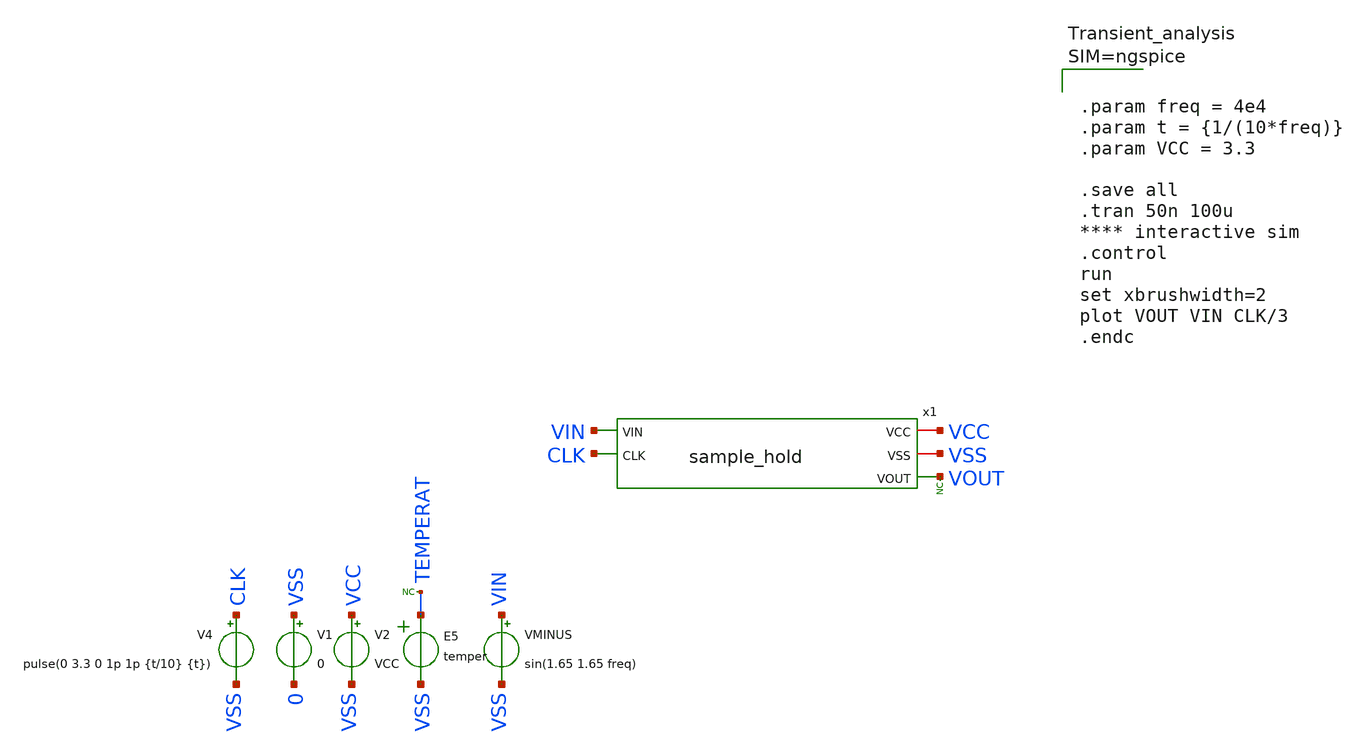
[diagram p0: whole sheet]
** sch_path: sample_hold/schematic/sample_hold_tb.sch
.lib $::SKYWATER_MODELS/sky130.lib.spice.tt.red tt
.include $::SKYWATER_STDCELLS/sky130_fd_sc_hd.spice

**.subckt sample_hold_tb
x1 VCC VSS VOUT VIN CLK sample_hold
V1 VSS 0 0
V2 VCC VSS VCC
VMINUS VIN VSS sin(1.65 1.65 freq)
E5 TEMPERAT VSS VOL=' temper '
* noconn TEMPERAT
V4 CLK VSS pulse(0 3.3 0 1p 1p {t/10} {t})
* noconn VOUT
**** begin user architecture code



.param freq = 4e4
.param t = {1/(10*freq)}
.param VCC = 3.3

.save all
.tran 50n 100u
**** interactive sim
.control
run
set xbrushwidth=2
plot VOUT VIN CLK/3
.endc



**** end user architecture code
**.ends

* expanding   symbol:  sample_hold.sym # of pins=5
** sym_path: sample_hold/schematic/sample_hold.sym
** sch_path: sample_hold/schematic/sample_hold.sch
.subckt sample_hold VCC VSS VOUT VIN CLK
*.iopin VCC
*.ipin VIN
*.opin VOUT
*.ipin CLK
*.iopin VSS
XM5 net1 net4 VCC VCC sky130_fd_pr__pfet_g5v0d10v5 L=0.5 W=1 nf=1 ad='int((nf+1)/2) * W/nf * 0.29' as='int((nf+2)/2) * W/nf * 0.29'
+ pd='2*int((nf+1)/2) * (W/nf + 0.29)' ps='2*int((nf+2)/2) * (W/nf + 0.29)' nrd='0.29 / W' nrs='0.29 / W'
+ sa=0 sb=0 sd=0 mult=1 m=1
XM6 net3 CLKN VSS VSS sky130_fd_pr__nfet_g5v0d10v5 L=0.5 W=1 nf=1 ad='int((nf+1)/2) * W/nf * 0.29' as='int((nf+2)/2) * W/nf * 0.29'
+ pd='2*int((nf+1)/2) * (W/nf + 0.29)' ps='2*int((nf+2)/2) * (W/nf + 0.29)' nrd='0.29 / W' nrs='0.29 / W'
+ sa=0 sb=0 sd=0 mult=1 m=1
XMa net2 CLK net3 VSS sky130_fd_pr__nfet_g5v0d10v5 L=0.5 W=1 nf=1 ad='int((nf+1)/2) * W/nf * 0.29' as='int((nf+2)/2) * W/nf * 0.29'
+ pd='2*int((nf+1)/2) * (W/nf + 0.29)' ps='2*int((nf+2)/2) * (W/nf + 0.29)' nrd='0.29 / W' nrs='0.29 / W'
+ sa=0 sb=0 sd=0 mult=1 m=1
XMb net2 CLK VCC VCC sky130_fd_pr__pfet_g5v0d10v5 L=0.5 W=1 nf=1 ad='int((nf+1)/2) * W/nf * 0.29' as='int((nf+2)/2) * W/nf * 0.29'
+ pd='2*int((nf+1)/2) * (W/nf + 0.29)' ps='2*int((nf+2)/2) * (W/nf + 0.29)' nrd='0.29 / W' nrs='0.29 / W'
+ sa=0 sb=0 sd=0 mult=1 m=1
XMc net2 net4 net3 VSS sky130_fd_pr__nfet_g5v0d10v5 L=0.5 W=1 nf=1 ad='int((nf+1)/2) * W/nf * 0.29' as='int((nf+2)/2) * W/nf * 0.29'
+ pd='2*int((nf+1)/2) * (W/nf + 0.29)' ps='2*int((nf+2)/2) * (W/nf + 0.29)' nrd='0.29 / W' nrs='0.29 / W'
+ sa=0 sb=0 sd=0 mult=1 m=1
XM2 net4 net2 net1 VCC sky130_fd_pr__pfet_g5v0d10v5 L=0.5 W=1 nf=1 ad='int((nf+1)/2) * W/nf * 0.29' as='int((nf+2)/2) * W/nf * 0.29'
+ pd='2*int((nf+1)/2) * (W/nf + 0.29)' ps='2*int((nf+2)/2) * (W/nf + 0.29)' nrd='0.29 / W' nrs='0.29 / W'
+ sa=0 sb=0 sd=0 mult=1 m=1
XM3 VIN net4 net3 VSS sky130_fd_pr__nfet_g5v0d10v5 L=0.5 W=1 nf=1 ad='int((nf+1)/2) * W/nf * 0.29' as='int((nf+2)/2) * W/nf * 0.29'
+ pd='2*int((nf+1)/2) * (W/nf + 0.29)' ps='2*int((nf+2)/2) * (W/nf + 0.29)' nrd='0.29 / W' nrs='0.29 / W'
+ sa=0 sb=0 sd=0 mult=1 m=1
XM8 net4 VCC net5 VSS sky130_fd_pr__nfet_g5v0d10v5 L=0.5 W=1 nf=1 ad='int((nf+1)/2) * W/nf * 0.29' as='int((nf+2)/2) * W/nf * 0.29'
+ pd='2*int((nf+1)/2) * (W/nf + 0.29)' ps='2*int((nf+2)/2) * (W/nf + 0.29)' nrd='0.29 / W' nrs='0.29 / W'
+ sa=0 sb=0 sd=0 mult=1 m=1
XM4 net5 CLKN VSS VSS sky130_fd_pr__nfet_g5v0d10v5 L=0.5 W=1 nf=1 ad='int((nf+1)/2) * W/nf * 0.29' as='int((nf+2)/2) * W/nf * 0.29'
+ pd='2*int((nf+1)/2) * (W/nf + 0.29)' ps='2*int((nf+2)/2) * (W/nf + 0.29)' nrd='0.29 / W' nrs='0.29 / W'
+ sa=0 sb=0 sd=0 mult=1 m=1
XM1 VOUT net4 VIN VSS sky130_fd_pr__nfet_g5v0d10v5 L=0.5 W=1 nf=2 ad='int((nf+1)/2) * W/nf * 0.29' as='int((nf+2)/2) * W/nf * 0.29'
+ pd='2*int((nf+1)/2) * (W/nf + 0.29)' ps='2*int((nf+2)/2) * (W/nf + 0.29)' nrd='0.29 / W' nrs='0.29 / W'
+ sa=0 sb=0 sd=0 mult=1 m=1
XM7 VOUT net6 VIN VCC sky130_fd_pr__pfet_g5v0d10v5 L=0.5 W=1 nf=1 ad='int((nf+1)/2) * W/nf * 0.29' as='int((nf+2)/2) * W/nf * 0.29'
+ pd='2*int((nf+1)/2) * (W/nf + 0.29)' ps='2*int((nf+2)/2) * (W/nf + 0.29)' nrd='0.29 / W' nrs='0.29 / W'
+ sa=0 sb=0 sd=0 mult=1 m=1
XMa1 net6 net4 VSS VSS sky130_fd_pr__nfet_g5v0d10v5 L=0.5 W=1 nf=1 ad='int((nf+1)/2) * W/nf * 0.29' as='int((nf+2)/2) * W/nf * 0.29'
+ pd='2*int((nf+1)/2) * (W/nf + 0.29)' ps='2*int((nf+2)/2) * (W/nf + 0.29)' nrd='0.29 / W' nrs='0.29 / W'
+ sa=0 sb=0 sd=0 mult=1 m=1
XMb2 net6 net4 VCC VCC sky130_fd_pr__pfet_g5v0d10v5 L=0.5 W=1 nf=1 ad='int((nf+1)/2) * W/nf * 0.29' as='int((nf+2)/2) * W/nf * 0.29'
+ pd='2*int((nf+1)/2) * (W/nf + 0.29)' ps='2*int((nf+2)/2) * (W/nf + 0.29)' nrd='0.29 / W' nrs='0.29 / W'
+ sa=0 sb=0 sd=0 mult=1 m=1
XC1 VOUT VSS sky130_fd_pr__cap_mim_m3_1 W=10 L=10 MF=2 m=2
XC2 net1 net3 sky130_fd_pr__cap_mim_m3_1 W=10 L=10 MF=2 m=2
XMa2 CLKN CLK VSS VSS sky130_fd_pr__nfet_g5v0d10v5 L=0.5 W=1 nf=1 ad='int((nf+1)/2) * W/nf * 0.29' as='int((nf+2)/2) * W/nf * 0.29'
+ pd='2*int((nf+1)/2) * (W/nf + 0.29)' ps='2*int((nf+2)/2) * (W/nf + 0.29)' nrd='0.29 / W' nrs='0.29 / W'
+ sa=0 sb=0 sd=0 mult=1 m=1
XMb3 CLKN CLK VCC VCC sky130_fd_pr__pfet_g5v0d10v5 L=0.5 W=1 nf=1 ad='int((nf+1)/2) * W/nf * 0.29' as='int((nf+2)/2) * W/nf * 0.29'
+ pd='2*int((nf+1)/2) * (W/nf + 0.29)' ps='2*int((nf+2)/2) * (W/nf + 0.29)' nrd='0.29 / W' nrs='0.29 / W'
+ sa=0 sb=0 sd=0 mult=1 m=1
.ends

.end
